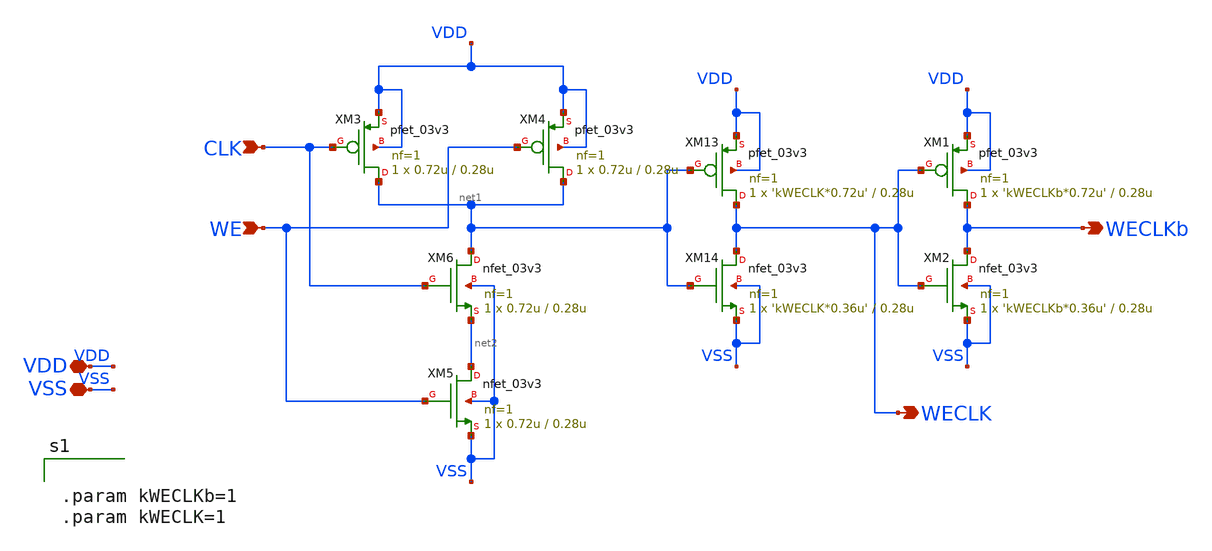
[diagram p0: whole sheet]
** sch_path: CAD3/driver_cell.sch
**.subckt driver_cell CLK WE VSS VDD WECLKb WECLK
*.ipin CLK
*.ipin WE
*.iopin VSS
*.iopin VDD
*.opin WECLKb
*.opin WECLK
XM13 WECLK net1 VDD VDD pfet_03v3 L=0.28u W='kWECLK*0.72u' nf=1 ad='int((nf+1)/2) * W/nf * 0.18u' as='int((nf+2)/2) * W/nf * 0.18u'
+ pd='2*int((nf+1)/2) * (W/nf + 0.18u)' ps='2*int((nf+2)/2) * (W/nf + 0.18u)' nrd='0.18u / W' nrs='0.18u / W'
+ sa=0 sb=0 sd=0 m=1
XM14 WECLK net1 VSS VSS nfet_03v3 L=0.28u W='kWECLK*0.36u' nf=1 ad='int((nf+1)/2) * W/nf * 0.18u' as='int((nf+2)/2) * W/nf * 0.18u'
+ pd='2*int((nf+1)/2) * (W/nf + 0.18u)' ps='2*int((nf+2)/2) * (W/nf + 0.18u)' nrd='0.18u / W' nrs='0.18u / W'
+ sa=0 sb=0 sd=0 m=1
XM1 WECLKb WECLK VDD VDD pfet_03v3 L=0.28u W='kWECLKb*0.72u' nf=1 ad='int((nf+1)/2) * W/nf * 0.18u' as='int((nf+2)/2) * W/nf * 0.18u'
+ pd='2*int((nf+1)/2) * (W/nf + 0.18u)' ps='2*int((nf+2)/2) * (W/nf + 0.18u)' nrd='0.18u / W' nrs='0.18u / W'
+ sa=0 sb=0 sd=0 m=1
XM2 WECLKb WECLK VSS VSS nfet_03v3 L=0.28u W='kWECLKb*0.36u' nf=1 ad='int((nf+1)/2) * W/nf * 0.18u' as='int((nf+2)/2) * W/nf * 0.18u'
+ pd='2*int((nf+1)/2) * (W/nf + 0.18u)' ps='2*int((nf+2)/2) * (W/nf + 0.18u)' nrd='0.18u / W' nrs='0.18u / W'
+ sa=0 sb=0 sd=0 m=1
XM3 net1 CLK VDD VDD pfet_03v3 L=0.28u W=0.72u nf=1 ad='int((nf+1)/2) * W/nf * 0.18u' as='int((nf+2)/2) * W/nf * 0.18u'
+ pd='2*int((nf+1)/2) * (W/nf + 0.18u)' ps='2*int((nf+2)/2) * (W/nf + 0.18u)' nrd='0.18u / W' nrs='0.18u / W'
+ sa=0 sb=0 sd=0 m=1
XM4 net1 WE VDD VDD pfet_03v3 L=0.28u W=0.72u nf=1 ad='int((nf+1)/2) * W/nf * 0.18u' as='int((nf+2)/2) * W/nf * 0.18u'
+ pd='2*int((nf+1)/2) * (W/nf + 0.18u)' ps='2*int((nf+2)/2) * (W/nf + 0.18u)' nrd='0.18u / W' nrs='0.18u / W'
+ sa=0 sb=0 sd=0 m=1
XM5 net2 WE VSS VSS nfet_03v3 L=0.28u W=0.72u nf=1 ad='int((nf+1)/2) * W/nf * 0.18u' as='int((nf+2)/2) * W/nf * 0.18u'
+ pd='2*int((nf+1)/2) * (W/nf + 0.18u)' ps='2*int((nf+2)/2) * (W/nf + 0.18u)' nrd='0.18u / W' nrs='0.18u / W'
+ sa=0 sb=0 sd=0 m=1
XM6 net1 CLK net2 VSS nfet_03v3 L=0.28u W=0.72u nf=1 ad='int((nf+1)/2) * W/nf * 0.18u' as='int((nf+2)/2) * W/nf * 0.18u'
+ pd='2*int((nf+1)/2) * (W/nf + 0.18u)' ps='2*int((nf+2)/2) * (W/nf + 0.18u)' nrd='0.18u / W' nrs='0.18u / W'
+ sa=0 sb=0 sd=0 m=1
**** begin user architecture code


.param kWECLKb=1
.param kWECLK=1


**** end user architecture code
**.ends
.end
